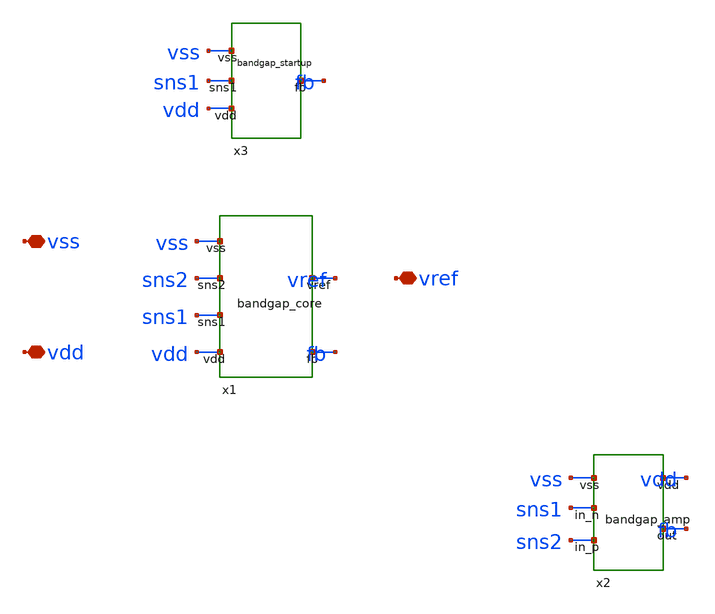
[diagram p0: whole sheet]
** sch_path: designs/g1-guardian/blocks/g1_bgr/source/2AMLogic-sg13g2-bandgap/bandgap_top.sch
**.subckt bandgap_top vdd vss vref
*.iopin vdd
*.iopin vss
*.iopin vref
Xx1 vdd vss fb sns1 sns2 vref bandgap_core
Xx2 sns2 sns1 vss fb vdd bandgap_amp
Xx3 vdd vss sns1 fb bandgap_startup
**.ends

* expanding   symbol:  bandgap_core.sym # of pins=6
** sym_path: bandgap_core.sym
** sch_path: bandgap_core.sch
.subckt bandgap_core vdd vss fb sns1 sns2 vref

*.iopin vdd
*.iopin vss
*.iopin fb
*.iopin sns1
*.iopin sns2
*.iopin vref
XM1 sns1 fb vdd vdd sg13_hv_pmos w=10u l=1u ng=1 m=1 mm_ok=1
XQ1 sns1 sns1 vss vss npn13G2 Nx=1 mm_ok=1
XM2A sns2 fb vdd vdd sg13_hv_pmos w=9u l=1u ng=1 m=1 mm_ok=1
XM2B sns2 fb vdd vdd sg13_hv_pmos w=1u l=1u ng=1 m=1 mm_ok=1
XR2 sns2 cb2 sub! rppd w=2u l=82.7u m=1 b=0 mm_ok=1
XQ2 cb2 cb2 vss vss npn13G2 Nx=8 mm_ok=1
XM3A vref fb vdd vdd sg13_hv_pmos w=8u l=1u ng=1 m=1 mm_ok=1
XM3B vref fb vdd vdd sg13_hv_pmos w=1u l=1u ng=1 m=1 mm_ok=1
XM3C vref fb vdd vdd sg13_hv_pmos w=1u l=1u ng=1 m=1 mm_ok=1
XR1 vref cb3 sub! rppd w=2u l=511u m=1 b=0 mm_ok=1
XQ3 cb3 cb3 vss vss npn13G2 Nx=1 mm_ok=1
.ends


* expanding   symbol:  bandgap_amp.sym # of pins=5
** sym_path: bandgap_amp.sym
** sch_path: bandgap_amp.sch
.subckt bandgap_amp in_p in_n vss out vdd

*.iopin vdd
*.iopin vss
*.iopin in_p
*.iopin in_n
*.iopin out
XMTAIL tail out vdd vdd sg13_hv_pmos w=10u l=1u ng=1 m=1 mm_ok=1
XMP1 d1 in_p tail vdd sg13_hv_pmos w=20u l=1u ng=1 m=1 mm_ok=1
XMP2 d2 in_n tail vdd sg13_hv_pmos w=20u l=1u ng=1 m=1 mm_ok=1
XMP3 pn pn vdd vdd sg13_hv_pmos w=10u l=1u ng=1 m=1 mm_ok=1
XMP4 out pn vdd vdd sg13_hv_pmos w=10u l=1u ng=1 m=1 mm_ok=1
XMN1 d1 d1 vss vss sg13_hv_nmos w=10u l=1u ng=1 m=1 mm_ok=1
XMN2 d2 d2 vss vss sg13_hv_nmos w=10u l=1u ng=1 m=1 mm_ok=1
XMN3 out d1 vss vss sg13_hv_nmos w=10u l=1u ng=1 m=1 mm_ok=1
XMN4 pn d2 vss vss sg13_hv_nmos w=10u l=1u ng=1 m=1 mm_ok=1
.ends


* expanding   symbol:  bandgap_startup.sym # of pins=4
** sym_path: bandgap_startup.sym
** sch_path: bandgap_startup.sch
.subckt bandgap_startup vdd vss sns1 fb

*.iopin vdd
*.iopin vss
*.iopin sns1
*.iopin fb
XRPU vdd det sub! rhigh w=1u l=1411.3u m=1 b=0 mm_ok=1
XMSENSE det sns1 vss vss sg13_hv_nmos w=10u l=0.5u ng=1 m=1 mm_ok=1
XMKFB fb det vss vss sg13_hv_nmos w=2u l=0.5u ng=1 m=1 mm_ok=1
.ends

.end
